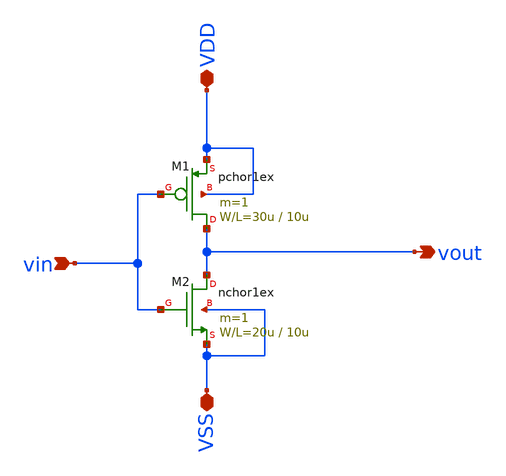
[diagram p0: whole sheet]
** sch_path: member_project/kensukeyama/katsuhito/Inverter_test3.sch
**.subckt Inverter_test3 vin VDD VSS vout
*.ipin vin
*.iopin VDD
*.iopin VSS
*.opin vout
M1 vout vin VDD VDD pchor1ex L=10u W=30u m=1
M2 vout vin VSS VSS nchor1ex L=10u W=20u m=1
**.ends
.end
